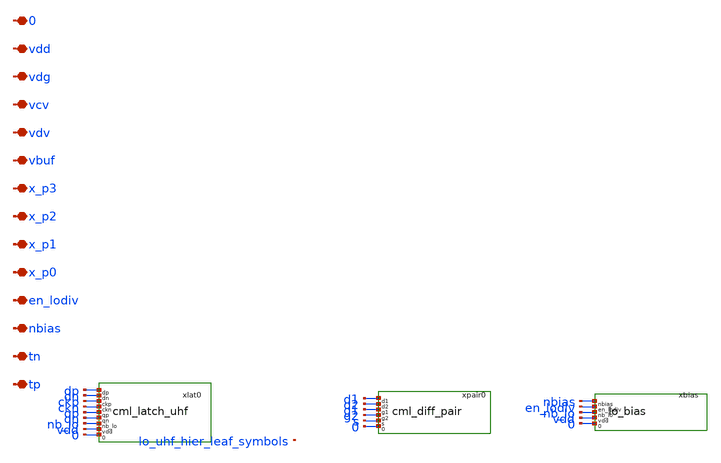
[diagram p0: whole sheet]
** sch_path: analog/lo/sch/lo_uhf_hier.sch
**.subckt lo_uhf_hier tp tn nbias en_lodiv x_p0 x_p1 x_p2 x_p3 vbuf vdv vcv vdg vdd 0
*.iopin tp
*.iopin tn
*.iopin nbias
*.iopin en_lodiv
*.iopin x_p0
*.iopin x_p1
*.iopin x_p2
*.iopin x_p3
*.iopin vbuf
*.iopin vdv
*.iopin vcv
*.iopin vdg
*.iopin vdd
*.iopin 0
xlat0 dp dn ckp ckn qp qn nb_lo vdd 0 cml_latch_uhf
xpair0 d1 d2 g1 g2 s 0 cml_diff_pair
xbias nbias en_lodiv nb_lo vdd 0 lo_bias
**.ends

* expanding   symbol:  cml_latch_uhf.sym # of pins=9
** sym_path: analog/lo/sch/cml_latch_uhf.sym
** sch_path: analog/lo/sch/cml_latch_uhf.sch
.subckt cml_latch_uhf dp dn ckp ckn qp qn nb_lo vdd 0
*.iopin dp
*.iopin dn
*.iopin ckp
*.iopin ckn
*.iopin qp
*.iopin qn
*.iopin nb_lo
*.iopin vdd
*.iopin 0
rlap vdd qp 666.7 m=1
rlan vdd qn 666.7 m=1
Xma1 qn dp s1a 0 sg13_lv_nmos w=7.50u l=0.13u ng=1 m=1 mm_ok=1
Xma2 qp dn s1a 0 sg13_lv_nmos w=7.50u l=0.13u ng=1 m=1 mm_ok=1
Xma3 qn qp s2a 0 sg13_lv_nmos w=11.25u l=0.13u ng=1 m=1 mm_ok=1
Xma4 qp qn s2a 0 sg13_lv_nmos w=11.25u l=0.13u ng=1 m=1 mm_ok=1
Xma5 s1a ckp ta 0 sg13_lv_nmos w=7.50u l=0.13u ng=1 m=1 mm_ok=1
Xma6 s2a ckn ta 0 sg13_lv_nmos w=7.50u l=0.13u ng=1 m=1 mm_ok=1
Xmta ta nb_lo 0 0 sg13_lv_nmos w=15u l=0.13u ng=1 m=1 mm_ok=1
.ends


* expanding   symbol:  cml_diff_pair.sym # of pins=6
** sym_path: analog/lo/sch/cml_diff_pair.sym
** sch_path: analog/lo/sch/cml_diff_pair.sch
.subckt cml_diff_pair d1 d2 g1 g2 s 0
*.iopin d1
*.iopin d2
*.iopin g1
*.iopin g2
*.iopin s
*.iopin 0
Xmm1 d1 g1 s 0 sg13_lv_nmos w=7.50u l=0.13u ng=1 m=1 mm_ok=1
Xmm2 d2 g2 s 0 sg13_lv_nmos w=7.50u l=0.13u ng=1 m=1 mm_ok=1
.ends


* expanding   symbol:  lo_bias.sym # of pins=5
** sym_path: analog/lo/sch/lo_bias.sym
** sch_path: analog/lo/sch/lo_bias.sch
.subckt lo_bias nbias en_lodiv nb_lo vdd 0
*.iopin nbias
*.iopin en_lodiv
*.iopin nb_lo
*.iopin vdd
*.iopin 0
Xxenb_p en_n en_lodiv vdd vdd sg13_lv_pmos w=1u l=0.13u ng=1 m=1 mm_ok=1
Xxenb_n en_n en_lodiv 0 0 sg13_lv_nmos w=0.5u l=0.13u ng=1 m=1 mm_ok=1
Xtgn nb_lo en_lodiv nbias 0 sg13_lv_nmos w=4u l=0.13u ng=1 m=1 mm_ok=1
Xtgp nb_lo en_n nbias vdd sg13_lv_pmos w=8u l=0.13u ng=1 m=1 mm_ok=1
Xmpd nb_lo en_n 0 0 sg13_lv_nmos w=2u l=0.13u ng=1 m=1 mm_ok=1
.ends

.end
